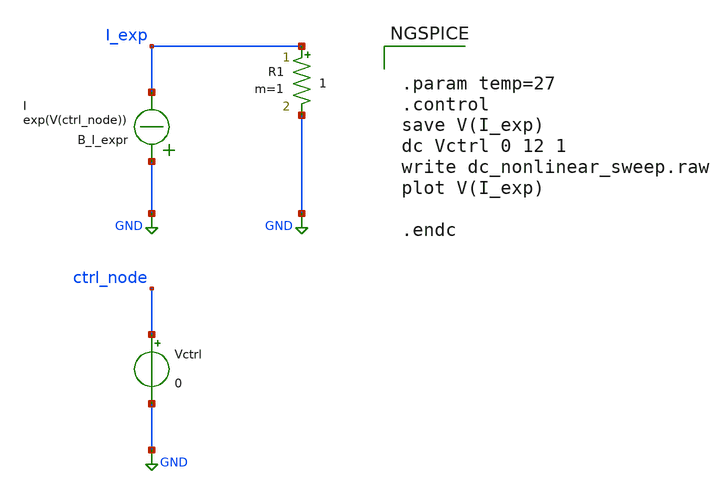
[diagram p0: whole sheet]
** sch_path: test_bench_temp/dc_nonlinear_sweep.sch
**.subckt dc_nonlinear_sweep
B_I_expr GND I_exp I = exp(V(ctrl_node))
Vctrl ctrl_node GND 0
R1 I_exp GND 1 m=1
**** begin user architecture code


.param temp=27
.control
save V(I_exp)
dc Vctrl 0 12 1
write dc_nonlinear_sweep.raw
plot V(I_exp)

.endc


**** end user architecture code
**.ends
.GLOBAL GND
.end
